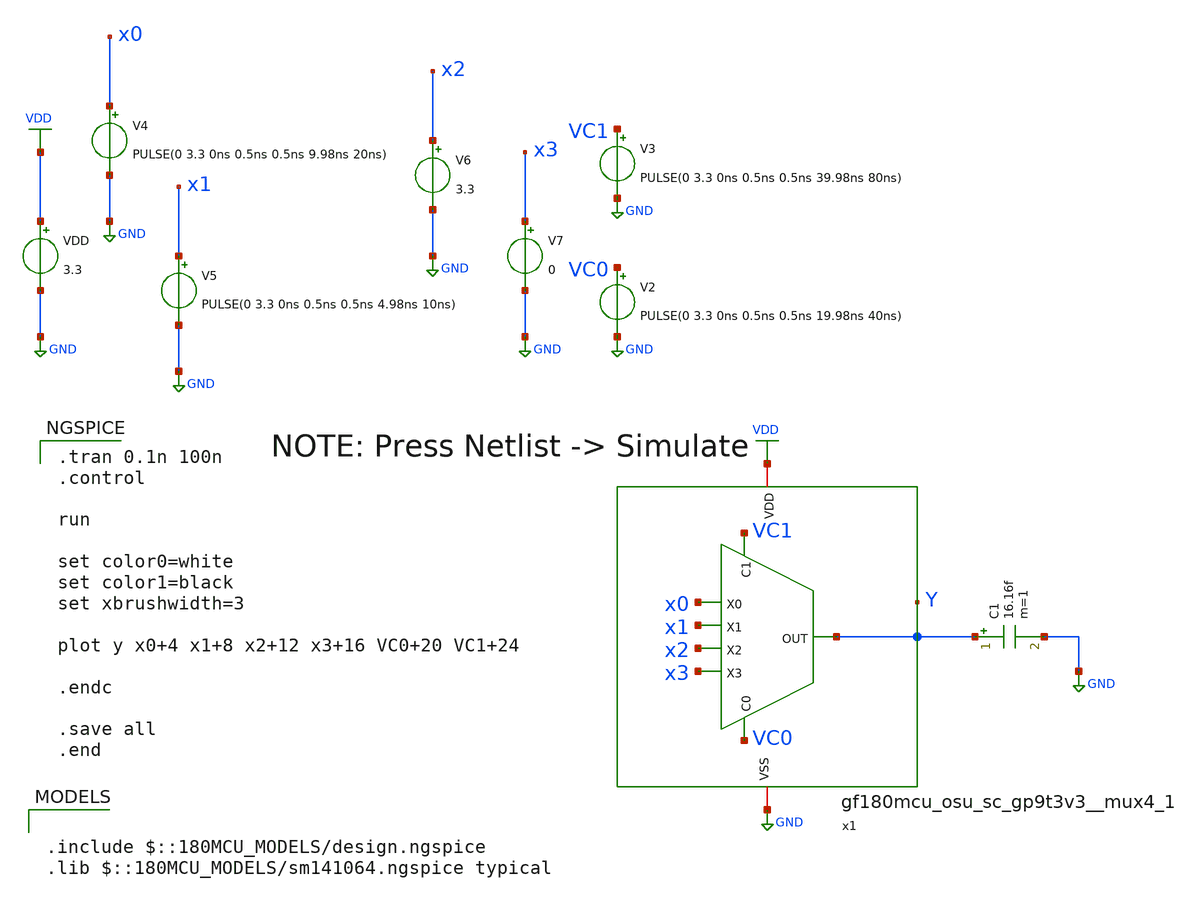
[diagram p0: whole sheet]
** sch_path: designs/MUX4/Schematic/gf180mcu_osu_sc_gp9t3v3__mux4_1_tb.sch
**.subckt gf180mcu_osu_sc_gp9t3v3__mux4_1_tb
VDD VDD GND 3.3
V2 VC0 GND PULSE(0 3.3 0ns 0.5ns 0.5ns 19.98ns 40ns)
V3 VC1 GND PULSE(0 3.3 0ns 0.5ns 0.5ns 39.98ns 80ns)
V4 x0 GND PULSE(0 3.3 0ns 0.5ns 0.5ns 9.98ns 20ns)
V5 x1 GND PULSE(0 3.3 0ns 0.5ns 0.5ns 4.98ns 10ns)
V6 x2 GND 3.3
V7 x3 GND 0
C1 Y GND 16.16f m=1
x1 VDD VC1 VC0 GND x0 x1 Y x2 x3 gf180mcu_osu_sc_gp9t3v3__mux4_1
**** begin user architecture code

.include $::180MCU_MODELS/design.ngspice
.lib $::180MCU_MODELS/sm141064.ngspice typical


.tran 0.1n 100n
.control

run

set color0=white
set color1=black
set xbrushwidth=3

plot y x0+4 x1+8 x2+12 x3+16 VC0+20 VC1+24

.endc

.save all
.end

**** end user architecture code
**.ends
.GLOBAL VDD
.GLOBAL GND
.end
